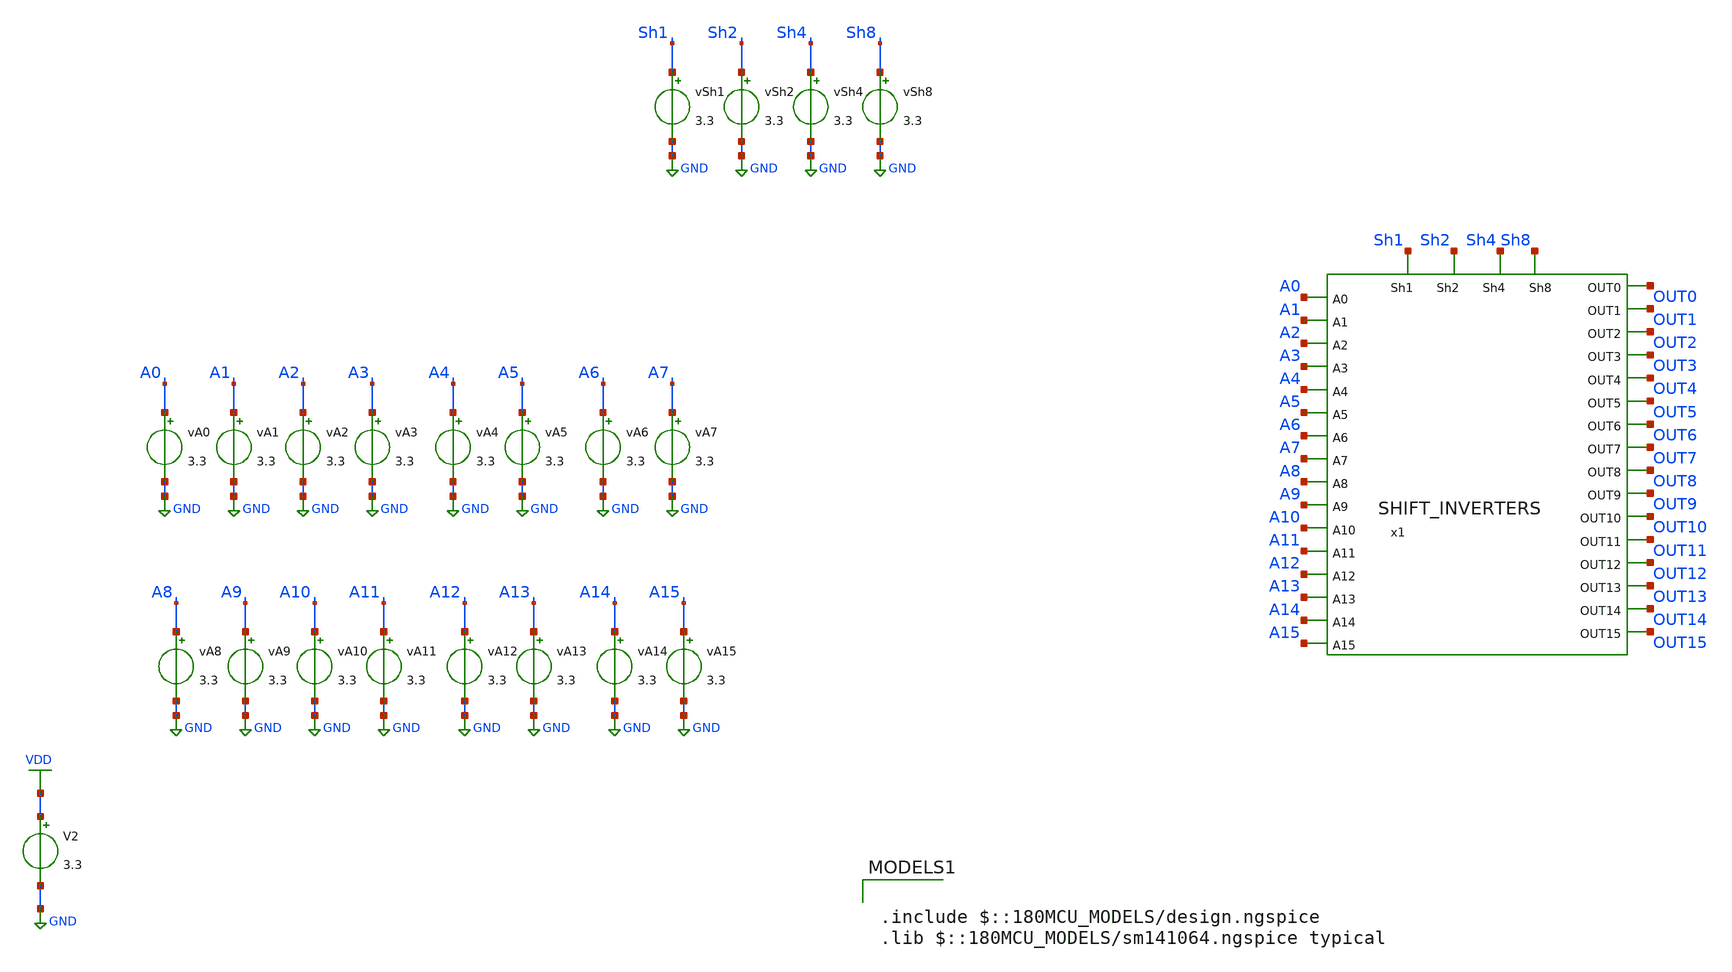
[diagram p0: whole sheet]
** sch_path: tbs/shift_tb_7_to13.sch
**.subckt shift_tb_7_to13
x1 OUT0 Sh1 OUT1 OUT2 Sh2 OUT3 OUT4 A0 OUT5 A1 OUT6 Sh4 OUT7 OUT8 A2 A3 OUT9 OUT10 OUT11 Sh8 OUT12
+ A4 OUT13 A5 A6 OUT14 A7 OUT15 A8 A9 A10 A11 A12 A13 A14 A15 SHIFT_INVERTERS
vA0 A0 GND 3.3
vA1 A1 GND 3.3
vA2 A2 GND 3.3
vA3 A3 GND 3.3
vA4 A4 GND 3.3
vA5 A5 GND 3.3
vA6 A6 GND 3.3
vA7 A7 GND 3.3
vA8 A8 GND 3.3
vA9 A9 GND 3.3
vA10 A10 GND 3.3
vA11 A11 GND 3.3
vA12 A12 GND 3.3
vA13 A13 GND 3.3
vA14 A14 GND 3.3
vA15 A15 GND 3.3
vSh1 Sh1 GND 3.3
vSh2 Sh2 GND 3.3
vSh4 Sh4 GND 3.3
vSh8 Sh8 GND 3.3
V2 VDD GND 3.3
**** begin user architecture code

.include $::180MCU_MODELS/design.ngspice
.lib $::180MCU_MODELS/sm141064.ngspice typical



.control
let vlow = 0
let vhigh = 3.3
* A = 1010101010101010 = 43690
alter VA15 = $&vhigh
alter VA14 = $&vlow
alter VA13 = $&vhigh
alter VA12 = $&vlow
alter VA11 = $&vhigh
alter VA10 = $&vlow
alter VA9  = $&vhigh
alter VA8  = $&vlow
alter VA7  = $&vhigh
alter VA6  = $&vlow
alter VA5  = $&vhigh
alter VA4  = $&vlow
alter VA3  = $&vhigh
alter VA2  = $&vlow
alter VA1  = $&vhigh
alter VA0  = $&vlow


* --- SHIFT 7 (0111) ---
alter vSh1 = $&vhigh
tran 1n 40n

meas tran v7_0  find v(OUT0)  at=30n
meas tran v7_1  find v(OUT1)  at=30n
meas tran v7_2  find v(OUT2)  at=30n
meas tran v7_3  find v(OUT3)  at=30n
meas tran v7_4  find v(OUT4)  at=30n
meas tran v7_5  find v(OUT5)  at=30n
meas tran v7_6  find v(OUT6)  at=30n
meas tran v7_7  find v(OUT7)  at=30n
meas tran v7_8  find v(OUT8)  at=30n
meas tran v7_9  find v(OUT9)  at=30n
meas tran v7_10 find v(OUT10) at=30n
meas tran v7_11 find v(OUT11) at=30n
meas tran v7_12 find v(OUT12) at=30n
meas tran v7_13 find v(OUT13) at=30n
meas tran v7_14 find v(OUT14) at=30n
meas tran v7_15 find v(OUT15) at=30n

let res7 = 0
if v7_0 > 1.6
  let res7 = res7 + 1
end
if v7_1 > 1.6
  let res7 = res7 + 2
end
if v7_2 > 1.6
  let res7 = res7 + 4
end
if v7_3 > 1.6
  let res7 = res7 + 8
end
if v7_4 > 1.6
  let res7 = res7 + 16
end
if v7_5 > 1.6
  let res7 = res7 + 32
end
if v7_6 > 1.6
  let res7 = res7 + 64
end
if v7_7 > 1.6
  let res7 = res7 + 128
end
if v7_8 > 1.6
  let res7 = res7 + 256
end
if v7_9 > 1.6
  let res7 = res7 + 512
end
if v7_10 > 1.6
  let res7 = res7 + 1024
end
if v7_11 > 1.6
  let res7 = res7 + 2048
end
if v7_12 > 1.6
  let res7 = res7 + 4096
end
if v7_13 > 1.6
  let res7 = res7 + 8192
end
if v7_14 > 1.6
  let res7 = res7 + 16384
end
if v7_15 > 1.6
  let res7 = res7 + 32768
end
echo 7_gives_21760
print res7

* --- SHIFT 8 (1000) ---
alter vSh1 = $&vlow
alter vSh2 = $&vlow
alter vSh4 = $&vlow
alter vSh8 = $&vhigh
tran 1n 40n

meas tran v8_0  find v(OUT0)  at=30n
meas tran v8_1  find v(OUT1)  at=30n
meas tran v8_2  find v(OUT2)  at=30n
meas tran v8_3  find v(OUT3)  at=30n
meas tran v8_4  find v(OUT4)  at=30n
meas tran v8_5  find v(OUT5)  at=30n
meas tran v8_6  find v(OUT6)  at=30n
meas tran v8_7  find v(OUT7)  at=30n
meas tran v8_8  find v(OUT8)  at=30n
meas tran v8_9  find v(OUT9)  at=30n
meas tran v8_10 find v(OUT10) at=30n
meas tran v8_11 find v(OUT11) at=30n
meas tran v8_12 find v(OUT12) at=30n
meas tran v8_13 find v(OUT13) at=30n
meas tran v8_14 find v(OUT14) at=30n
meas tran v8_15 find v(OUT15) at=30n

let res8 = 0
if v8_0 > 1.6
  let res8 = res8 + 1
end
if v8_1 > 1.6
  let res8 = res8 + 2
end
if v8_2 > 1.6
  let res8 = res8 + 4
end
if v8_3 > 1.6
  let res8 = res8 + 8
end
if v8_4 > 1.6
  let res8 = res8 + 16
end
if v8_5 > 1.6
  let res8 = res8 + 32
end
if v8_6 > 1.6
  let res8 = res8 + 64
end
if v8_7 > 1.6
  let res8 = res8 + 128
end
if v8_8 > 1.6
  let res8 = res8 + 256
end
if v8_9 > 1.6
  let res8 = res8 + 512
end
if v8_10 > 1.6
  let res8 = res8 + 1024
end
if v8_11 > 1.6
  let res8 = res8 + 2048
end
if v8_12 > 1.6
  let res8 = res8 + 4096
end
if v8_13 > 1.6
  let res8 = res8 + 8192
end
if v8_14 > 1.6
  let res8 = res8 + 16384
end
if v8_15 > 1.6
  let res8 = res8 + 32768
end
echo 8_gives_43520
print res8
* --- SHIFT 9 (1001) ---
alter vSh8 = $&vhigh
alter vSh4 = $&vlow
alter vSh2 = $&vlow
alter vSh1 = $&vhigh

tran 1n 40n

meas tran v9_0  find v(OUT0)  at=30n
meas tran v9_1  find v(OUT1)  at=30n
meas tran v9_2  find v(OUT2)  at=30n
meas tran v9_3  find v(OUT3)  at=30n
meas tran v9_4  find v(OUT4)  at=30n
meas tran v9_5  find v(OUT5)  at=30n
meas tran v9_6  find v(OUT6)  at=30n
meas tran v9_7  find v(OUT7)  at=30n
meas tran v9_8  find v(OUT8)  at=30n
meas tran v9_9  find v(OUT9)  at=30n
meas tran v9_10 find v(OUT10) at=30n
meas tran v9_11 find v(OUT11) at=30n
meas tran v9_12 find v(OUT12) at=30n
meas tran v9_13 find v(OUT13) at=30n
meas tran v9_14 find v(OUT14) at=30n
meas tran v9_15 find v(OUT15) at=30n

let res9 = 0
if v9_0 > 1.6
  let res9 = res9 + 1
end
if v9_1 > 1.6
  let res9 = res9 + 2
end
if v9_2 > 1.6
  let res9 = res9 + 4
end
if v9_3 > 1.6
  let res9 = res9 + 8
end
if v9_4 > 1.6
  let res9 = res9 + 16
end
if v9_5 > 1.6
  let res9 = res9 + 32
end
if v9_6 > 1.6
  let res9 = res9 + 64
end
if v9_7 > 1.6
  let res9 = res9 + 128
end
if v9_8 > 1.6
  let res9 = res9 + 256
end
if v9_9 > 1.6
  let res9 = res9 + 512
end
if v9_10 > 1.6
  let res9 = res9 + 1024
end
if v9_11 > 1.6
  let res9 = res9 + 2048
end
if v9_12 > 1.6
  let res9 = res9 + 4096
end
if v9_13 > 1.6
  let res9 = res9 + 8192
end
if v9_14 > 1.6
  let res9 = res9 + 16384
end
if v9_15 > 1.6
  let res9 = res9 + 32768
end
echo 9_gives_21504
print res9

* --- SHIFT 10 (1010) ---
alter vSh1 = $&vlow
alter vSh2 = $&vhigh
tran 1n 40n

meas tran v10_0  find v(OUT0)  at=30n
meas tran v10_1  find v(OUT1)  at=30n
meas tran v10_2  find v(OUT2)  at=30n
meas tran v10_3  find v(OUT3)  at=30n
meas tran v10_4  find v(OUT4)  at=30n
meas tran v10_5  find v(OUT5)  at=30n
meas tran v10_6  find v(OUT6)  at=30n
meas tran v10_7  find v(OUT7)  at=30n
meas tran v10_8  find v(OUT8)  at=30n
meas tran v10_9  find v(OUT9)  at=30n
meas tran v10_10 find v(OUT10) at=30n
meas tran v10_11 find v(OUT11) at=30n
meas tran v10_12 find v(OUT12) at=30n
meas tran v10_13 find v(OUT13) at=30n
meas tran v10_14 find v(OUT14) at=30n
meas tran v10_15 find v(OUT15) at=30n

let res10 = 0
if v10_0 > 1.6
  let res10 = res10 + 1
end
if v10_1 > 1.6
  let res10 = res10 + 2
end
if v10_2 > 1.6
  let res10 = res10 + 4
end
if v10_3 > 1.6
  let res10 = res10 + 8
end
if v10_4 > 1.6
  let res10 = res10 + 16
end
if v10_5 > 1.6
  let res10 = res10 + 32
end
if v10_6 > 1.6
  let res10 = res10 + 64
end
if v10_7 > 1.6
  let res10 = res10 + 128
end
if v10_8 > 1.6
  let res10 = res10 + 256
end
if v10_9 > 1.6
  let res10 = res10 + 512
end
if v10_10 > 1.6
  let res10 = res10 + 1024
end
if v10_11 > 1.6
  let res10 = res10 + 2048
end
if v10_12 > 1.6
  let res10 = res10 + 4096
end
if v10_13 > 1.6
  let res10 = res10 + 8192
end
if v10_14 > 1.6
  let res10 = res10 + 16384
end
if v10_15 > 1.6
  let res10 = res10 + 32768
end
echo 10_gives_43008
print res10

* --- SHIFT 11 (1011) ---
alter vSh1 = $&vhigh
tran 1n 40n

meas tran v11_0  find v(OUT0)  at=30n
meas tran v11_1  find v(OUT1)  at=30n
meas tran v11_2  find v(OUT2)  at=30n
meas tran v11_3  find v(OUT3)  at=30n
meas tran v11_4  find v(OUT4)  at=30n
meas tran v11_5  find v(OUT5)  at=30n
meas tran v11_6  find v(OUT6)  at=30n
meas tran v11_7  find v(OUT7)  at=30n
meas tran v11_8  find v(OUT8)  at=30n
meas tran v11_9  find v(OUT9)  at=30n
meas tran v11_10 find v(OUT10) at=30n
meas tran v11_11 find v(OUT11) at=30n
meas tran v11_12 find v(OUT12) at=30n
meas tran v11_13 find v(OUT13) at=30n
meas tran v11_14 find v(OUT14) at=30n
meas tran v11_15 find v(OUT15) at=30n

let res11 = 0
if v11_0 > 1.6
  let res11 = res11 + 1
end
if v11_1 > 1.6
  let res11 = res11 + 2
end
if v11_2 > 1.6
  let res11 = res11 + 4
end
if v11_3 > 1.6
  let res11 = res11 + 8
end
if v11_4 > 1.6
  let res11 = res11 + 16
end
if v11_5 > 1.6
  let res11 = res11 + 32
end
if v11_6 > 1.6
  let res11 = res11 + 64
end
if v11_7 > 1.6
  let res11 = res11 + 128
end
if v11_8 > 1.6
  let res11 = res11 + 256
end
if v11_9 > 1.6
  let res11 = res11 + 512
end
if v11_10 > 1.6
  let res11 = res11 + 1024
end
if v11_11 > 1.6
  let res11 = res11 + 2048
end
if v11_12 > 1.6
  let res11 = res11 + 4096
end
if v11_13 > 1.6
  let res11 = res11 + 8192
end
if v11_14 > 1.6
  let res11 = res11 + 16384
end
if v11_15 > 1.6
  let res11 = res11 + 32768
end
echo 11_gives_20480
print res11

* --- SHIFT 12 (1100) ---
alter vSh1 = $&vlow
alter vSh2 = $&vlow
alter vSh4 = $&vhigh
tran 1n 40n

meas tran v12_0  find v(OUT0)  at=30n
meas tran v12_1  find v(OUT1)  at=30n
meas tran v12_2  find v(OUT2)  at=30n
meas tran v12_3  find v(OUT3)  at=30n
meas tran v12_4  find v(OUT4)  at=30n
meas tran v12_5  find v(OUT5)  at=30n
meas tran v12_6  find v(OUT6)  at=30n
meas tran v12_7  find v(OUT7)  at=30n
meas tran v12_8  find v(OUT8)  at=30n
meas tran v12_9  find v(OUT9)  at=30n
meas tran v12_10 find v(OUT10) at=30n
meas tran v12_11 find v(OUT11) at=30n
meas tran v12_12 find v(OUT12) at=30n
meas tran v12_13 find v(OUT13) at=30n
meas tran v12_14 find v(OUT14) at=30n
meas tran v12_15 find v(OUT15) at=30n

let res12 = 0
if v12_0 > 1.6
  let res12 = res12 + 1
end
if v12_1 > 1.6
  let res12 = res12 + 2
end
if v12_2 > 1.6
  let res12 = res12 + 4
end
if v12_3 > 1.6
  let res12 = res12 + 8
end
if v12_4 > 1.6
  let res12 = res12 + 16
end
if v12_5 > 1.6
  let res12 = res12 + 32
end
if v12_6 > 1.6
  let res12 = res12 + 64
end
if v12_7 > 1.6
  let res12 = res12 + 128
end
if v12_8 > 1.6
  let res12 = res12 + 256
end
if v12_9 > 1.6
  let res12 = res12 + 512
end
if v12_10 > 1.6
  let res12 = res12 + 1024
end
if v12_11 > 1.6
  let res12 = res12 + 2048
end
if v12_12 > 1.6
  let res12 = res12 + 4096
end
if v12_13 > 1.6
  let res12 = res12 + 8192
end
if v12_14 > 1.6
  let res12 = res12 + 16384
end
if v12_15 > 1.6
  let res12 = res12 + 32768
end
echo 12_gives_40960
print res12
* --- SHIFT 13 (1101) ---
alter vSh8 = $&vhigh
alter vSh4 = $&vhigh
alter vSh2 = $&vlow
alter vSh1 = $&vhigh

tran 1n 40n

meas tran v13_0  find v(OUT0)  at=30n
meas tran v13_1  find v(OUT1)  at=30n
meas tran v13_2  find v(OUT2)  at=30n
meas tran v13_3  find v(OUT3)  at=30n
meas tran v13_4  find v(OUT4)  at=30n
meas tran v13_5  find v(OUT5)  at=30n
meas tran v13_6  find v(OUT6)  at=30n
meas tran v13_7  find v(OUT7)  at=30n
meas tran v13_8  find v(OUT8)  at=30n
meas tran v13_9  find v(OUT9)  at=30n
meas tran v13_10 find v(OUT10) at=30n
meas tran v13_11 find v(OUT11) at=30n
meas tran v13_12 find v(OUT12) at=30n
meas tran v13_13 find v(OUT13) at=30n
meas tran v13_14 find v(OUT14) at=30n
meas tran v13_15 find v(OUT15) at=30n

let res13 = 0
if v13_0 > 1.6
  let res13 = res13 + 1
end
if v13_1 > 1.6
  let res13 = res13 + 2
end
if v13_2 > 1.6
  let res13 = res13 + 4
end
if v13_3 > 1.6
  let res13 = res13 + 8
end
if v13_4 > 1.6
  let res13 = res13 + 16
end
if v13_5 > 1.6
  let res13 = res13 + 32
end
if v13_6 > 1.6
  let res13 = res13 + 64
end
if v13_7 > 1.6
  let res13 = res13 + 128
end
if v13_8 > 1.6
  let res13 = res13 + 256
end
if v13_9 > 1.6
  let res13 = res13 + 512
end
if v13_10 > 1.6
  let res13 = res13 + 1024
end
if v13_11 > 1.6
  let res13 = res13 + 2048
end
if v13_12 > 1.6
  let res13 = res13 + 4096
end
if v13_13 > 1.6
  let res13 = res13 + 8192
end
if v13_14 > 1.6
  let res13 = res13 + 16384
end
if v13_15 > 1.6
  let res13 = res13 + 32768
end
echo 13_gives_16384
print res13

.endc


**** end user architecture code
**.ends
.GLOBAL GND
.GLOBAL VDD
.end
